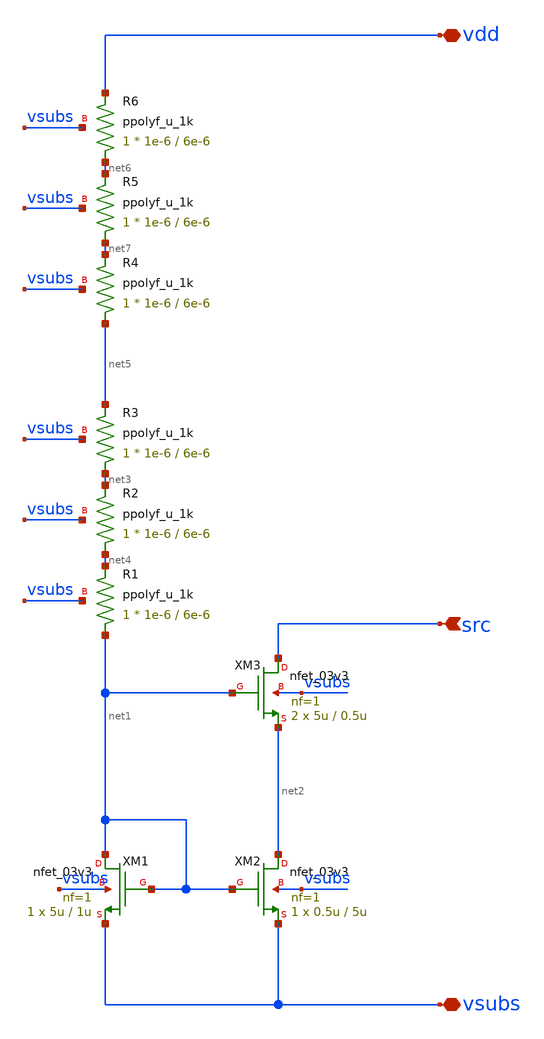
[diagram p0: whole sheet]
** sch_path: xschem/ip_current_source.sch
**.subckt ip_current_source vdd vsubs src
*.iopin vdd
*.iopin vsubs
*.ipin src
XM1 net1 net1 vsubs vsubs nfet_03v3 L=1u W=5u nf=1 ad='int((nf+1)/2) * W/nf * 0.18u' as='int((nf+2)/2) * W/nf * 0.18u'
+ pd='2*int((nf+1)/2) * (W/nf + 0.18u)' ps='2*int((nf+2)/2) * (W/nf + 0.18u)' nrd='0.18u / W' nrs='0.18u / W'
+ sa=0 sb=0 sd=0 m=1
XM2 net2 net1 vsubs vsubs nfet_03v3 L=5u W=0.5u nf=1 ad='int((nf+1)/2) * W/nf * 0.18u' as='int((nf+2)/2) * W/nf * 0.18u'
+ pd='2*int((nf+1)/2) * (W/nf + 0.18u)' ps='2*int((nf+2)/2) * (W/nf + 0.18u)' nrd='0.18u / W' nrs='0.18u / W'
+ sa=0 sb=0 sd=0 m=1
XM3 src net1 net2 vsubs nfet_03v3 L=0.5u W=5u nf=1 ad='int((nf+1)/2) * W/nf * 0.18u' as='int((nf+2)/2) * W/nf * 0.18u'
+ pd='2*int((nf+1)/2) * (W/nf + 0.18u)' ps='2*int((nf+2)/2) * (W/nf + 0.18u)' nrd='0.18u / W' nrs='0.18u / W'
+ sa=0 sb=0 sd=0 m=2
XR1 net1 net4 vsubs ppolyf_u_1k r_width=1e-6 r_length=6e-6 m=1
XR2 net4 net3 vsubs ppolyf_u_1k r_width=1e-6 r_length=6e-6 m=1
XR3 net3 net5 vsubs ppolyf_u_1k r_width=1e-6 r_length=6e-6 m=1
XR4 net5 net7 vsubs ppolyf_u_1k r_width=1e-6 r_length=6e-6 m=1
XR5 net7 net6 vsubs ppolyf_u_1k r_width=1e-6 r_length=6e-6 m=1
XR6 net6 vdd vsubs ppolyf_u_1k r_width=1e-6 r_length=6e-6 m=1
**.ends
.end
